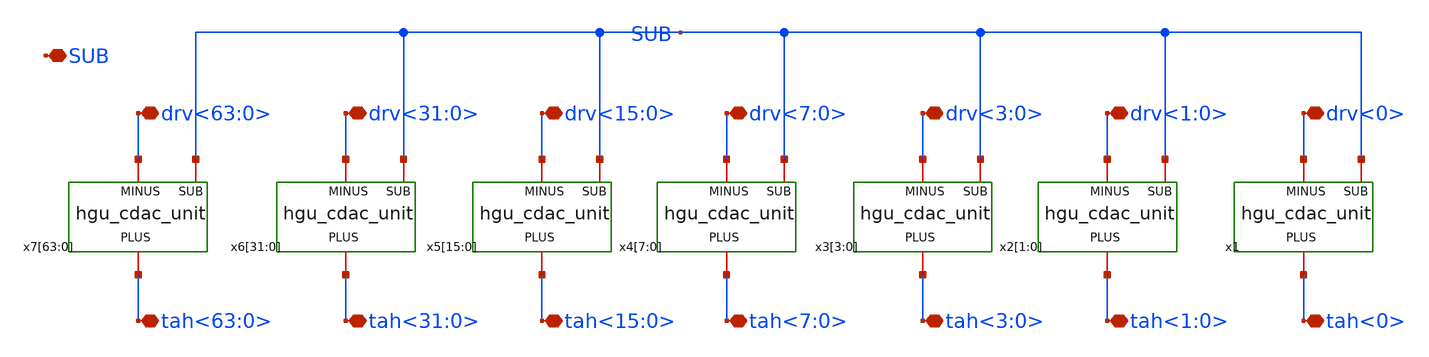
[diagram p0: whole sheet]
** sch_path: hgu/xschem/hgu_cdac_8bit_array.sch
**.subckt hgu_cdac_8bit_array drv<0> drv<1:0> drv<3:0> drv<7:0> drv<15:0> drv<31:0> drv<63:0> tah<0>
*+ tah<1:0> tah<3:0> tah<7:0> tah<15:0> tah<31:0> tah<63:0> SUB
*.iopin drv<0>
*.iopin drv<1:0>
*.iopin drv<3:0>
*.iopin drv<7:0>
*.iopin drv<15:0>
*.iopin drv<31:0>
*.iopin drv<63:0>
*.iopin tah<0>
*.iopin tah<1:0>
*.iopin tah<3:0>
*.iopin tah<7:0>
*.iopin tah<15:0>
*.iopin tah<31:0>
*.iopin tah<63:0>
*.iopin SUB
x1 tah<0> drv<0> SUB hgu_cdac_unit
x2[1] tah<1:0> drv<1:0> SUB hgu_cdac_unit
x2[0] tah<1:0> drv<1:0> SUB hgu_cdac_unit
x3[3] tah<3:0> drv<3:0> SUB hgu_cdac_unit
x3[2] tah<3:0> drv<3:0> SUB hgu_cdac_unit
x3[1] tah<3:0> drv<3:0> SUB hgu_cdac_unit
x3[0] tah<3:0> drv<3:0> SUB hgu_cdac_unit
x4[7] tah<7:0> drv<7:0> SUB hgu_cdac_unit
x4[6] tah<7:0> drv<7:0> SUB hgu_cdac_unit
x4[5] tah<7:0> drv<7:0> SUB hgu_cdac_unit
x4[4] tah<7:0> drv<7:0> SUB hgu_cdac_unit
x4[3] tah<7:0> drv<7:0> SUB hgu_cdac_unit
x4[2] tah<7:0> drv<7:0> SUB hgu_cdac_unit
x4[1] tah<7:0> drv<7:0> SUB hgu_cdac_unit
x4[0] tah<7:0> drv<7:0> SUB hgu_cdac_unit
x5[15] tah<15:0> drv<15:0> SUB hgu_cdac_unit
x5[14] tah<15:0> drv<15:0> SUB hgu_cdac_unit
x5[13] tah<15:0> drv<15:0> SUB hgu_cdac_unit
x5[12] tah<15:0> drv<15:0> SUB hgu_cdac_unit
x5[11] tah<15:0> drv<15:0> SUB hgu_cdac_unit
x5[10] tah<15:0> drv<15:0> SUB hgu_cdac_unit
x5[9] tah<15:0> drv<15:0> SUB hgu_cdac_unit
x5[8] tah<15:0> drv<15:0> SUB hgu_cdac_unit
x5[7] tah<15:0> drv<15:0> SUB hgu_cdac_unit
x5[6] tah<15:0> drv<15:0> SUB hgu_cdac_unit
x5[5] tah<15:0> drv<15:0> SUB hgu_cdac_unit
x5[4] tah<15:0> drv<15:0> SUB hgu_cdac_unit
x5[3] tah<15:0> drv<15:0> SUB hgu_cdac_unit
x5[2] tah<15:0> drv<15:0> SUB hgu_cdac_unit
x5[1] tah<15:0> drv<15:0> SUB hgu_cdac_unit
x5[0] tah<15:0> drv<15:0> SUB hgu_cdac_unit
x6[31] tah<31:0> drv<31:0> SUB hgu_cdac_unit
x6[30] tah<31:0> drv<31:0> SUB hgu_cdac_unit
x6[29] tah<31:0> drv<31:0> SUB hgu_cdac_unit
x6[28] tah<31:0> drv<31:0> SUB hgu_cdac_unit
x6[27] tah<31:0> drv<31:0> SUB hgu_cdac_unit
x6[26] tah<31:0> drv<31:0> SUB hgu_cdac_unit
x6[25] tah<31:0> drv<31:0> SUB hgu_cdac_unit
x6[24] tah<31:0> drv<31:0> SUB hgu_cdac_unit
x6[23] tah<31:0> drv<31:0> SUB hgu_cdac_unit
x6[22] tah<31:0> drv<31:0> SUB hgu_cdac_unit
x6[21] tah<31:0> drv<31:0> SUB hgu_cdac_unit
x6[20] tah<31:0> drv<31:0> SUB hgu_cdac_unit
x6[19] tah<31:0> drv<31:0> SUB hgu_cdac_unit
x6[18] tah<31:0> drv<31:0> SUB hgu_cdac_unit
x6[17] tah<31:0> drv<31:0> SUB hgu_cdac_unit
x6[16] tah<31:0> drv<31:0> SUB hgu_cdac_unit
x6[15] tah<31:0> drv<31:0> SUB hgu_cdac_unit
x6[14] tah<31:0> drv<31:0> SUB hgu_cdac_unit
x6[13] tah<31:0> drv<31:0> SUB hgu_cdac_unit
x6[12] tah<31:0> drv<31:0> SUB hgu_cdac_unit
x6[11] tah<31:0> drv<31:0> SUB hgu_cdac_unit
x6[10] tah<31:0> drv<31:0> SUB hgu_cdac_unit
x6[9] tah<31:0> drv<31:0> SUB hgu_cdac_unit
x6[8] tah<31:0> drv<31:0> SUB hgu_cdac_unit
x6[7] tah<31:0> drv<31:0> SUB hgu_cdac_unit
x6[6] tah<31:0> drv<31:0> SUB hgu_cdac_unit
x6[5] tah<31:0> drv<31:0> SUB hgu_cdac_unit
x6[4] tah<31:0> drv<31:0> SUB hgu_cdac_unit
x6[3] tah<31:0> drv<31:0> SUB hgu_cdac_unit
x6[2] tah<31:0> drv<31:0> SUB hgu_cdac_unit
x6[1] tah<31:0> drv<31:0> SUB hgu_cdac_unit
x6[0] tah<31:0> drv<31:0> SUB hgu_cdac_unit
x7[63] tah<63:0> drv<63:0> SUB hgu_cdac_unit
x7[62] tah<63:0> drv<63:0> SUB hgu_cdac_unit
x7[61] tah<63:0> drv<63:0> SUB hgu_cdac_unit
x7[60] tah<63:0> drv<63:0> SUB hgu_cdac_unit
x7[59] tah<63:0> drv<63:0> SUB hgu_cdac_unit
x7[58] tah<63:0> drv<63:0> SUB hgu_cdac_unit
x7[57] tah<63:0> drv<63:0> SUB hgu_cdac_unit
x7[56] tah<63:0> drv<63:0> SUB hgu_cdac_unit
x7[55] tah<63:0> drv<63:0> SUB hgu_cdac_unit
x7[54] tah<63:0> drv<63:0> SUB hgu_cdac_unit
x7[53] tah<63:0> drv<63:0> SUB hgu_cdac_unit
x7[52] tah<63:0> drv<63:0> SUB hgu_cdac_unit
x7[51] tah<63:0> drv<63:0> SUB hgu_cdac_unit
x7[50] tah<63:0> drv<63:0> SUB hgu_cdac_unit
x7[49] tah<63:0> drv<63:0> SUB hgu_cdac_unit
x7[48] tah<63:0> drv<63:0> SUB hgu_cdac_unit
x7[47] tah<63:0> drv<63:0> SUB hgu_cdac_unit
x7[46] tah<63:0> drv<63:0> SUB hgu_cdac_unit
x7[45] tah<63:0> drv<63:0> SUB hgu_cdac_unit
x7[44] tah<63:0> drv<63:0> SUB hgu_cdac_unit
x7[43] tah<63:0> drv<63:0> SUB hgu_cdac_unit
x7[42] tah<63:0> drv<63:0> SUB hgu_cdac_unit
x7[41] tah<63:0> drv<63:0> SUB hgu_cdac_unit
x7[40] tah<63:0> drv<63:0> SUB hgu_cdac_unit
x7[39] tah<63:0> drv<63:0> SUB hgu_cdac_unit
x7[38] tah<63:0> drv<63:0> SUB hgu_cdac_unit
x7[37] tah<63:0> drv<63:0> SUB hgu_cdac_unit
x7[36] tah<63:0> drv<63:0> SUB hgu_cdac_unit
x7[35] tah<63:0> drv<63:0> SUB hgu_cdac_unit
x7[34] tah<63:0> drv<63:0> SUB hgu_cdac_unit
x7[33] tah<63:0> drv<63:0> SUB hgu_cdac_unit
x7[32] tah<63:0> drv<63:0> SUB hgu_cdac_unit
x7[31] tah<63:0> drv<63:0> SUB hgu_cdac_unit
x7[30] tah<63:0> drv<63:0> SUB hgu_cdac_unit
x7[29] tah<63:0> drv<63:0> SUB hgu_cdac_unit
x7[28] tah<63:0> drv<63:0> SUB hgu_cdac_unit
x7[27] tah<63:0> drv<63:0> SUB hgu_cdac_unit
x7[26] tah<63:0> drv<63:0> SUB hgu_cdac_unit
x7[25] tah<63:0> drv<63:0> SUB hgu_cdac_unit
x7[24] tah<63:0> drv<63:0> SUB hgu_cdac_unit
x7[23] tah<63:0> drv<63:0> SUB hgu_cdac_unit
x7[22] tah<63:0> drv<63:0> SUB hgu_cdac_unit
x7[21] tah<63:0> drv<63:0> SUB hgu_cdac_unit
x7[20] tah<63:0> drv<63:0> SUB hgu_cdac_unit
x7[19] tah<63:0> drv<63:0> SUB hgu_cdac_unit
x7[18] tah<63:0> drv<63:0> SUB hgu_cdac_unit
x7[17] tah<63:0> drv<63:0> SUB hgu_cdac_unit
x7[16] tah<63:0> drv<63:0> SUB hgu_cdac_unit
x7[15] tah<63:0> drv<63:0> SUB hgu_cdac_unit
x7[14] tah<63:0> drv<63:0> SUB hgu_cdac_unit
x7[13] tah<63:0> drv<63:0> SUB hgu_cdac_unit
x7[12] tah<63:0> drv<63:0> SUB hgu_cdac_unit
x7[11] tah<63:0> drv<63:0> SUB hgu_cdac_unit
x7[10] tah<63:0> drv<63:0> SUB hgu_cdac_unit
x7[9] tah<63:0> drv<63:0> SUB hgu_cdac_unit
x7[8] tah<63:0> drv<63:0> SUB hgu_cdac_unit
x7[7] tah<63:0> drv<63:0> SUB hgu_cdac_unit
x7[6] tah<63:0> drv<63:0> SUB hgu_cdac_unit
x7[5] tah<63:0> drv<63:0> SUB hgu_cdac_unit
x7[4] tah<63:0> drv<63:0> SUB hgu_cdac_unit
x7[3] tah<63:0> drv<63:0> SUB hgu_cdac_unit
x7[2] tah<63:0> drv<63:0> SUB hgu_cdac_unit
x7[1] tah<63:0> drv<63:0> SUB hgu_cdac_unit
x7[0] tah<63:0> drv<63:0> SUB hgu_cdac_unit
**.ends

* expanding   symbol:  hgu_cdac_unit.sym # of pins=3
** sym_path: hgu/xschem/hgu_cdac_unit.sym
** sch_path: hgu/xschem/hgu_cdac_unit.sch
.subckt hgu_cdac_unit PLUS MINUS SUB  csize=1
*.iopin PLUS
*.iopin MINUS
*.iopin SUB
XC2 PLUS MINUS SUB sky130_fd_pr__cap_vpp_02p4x04p6_m1m2_noshield mult=1 m=1
* noconn #net1
.ends

.end
